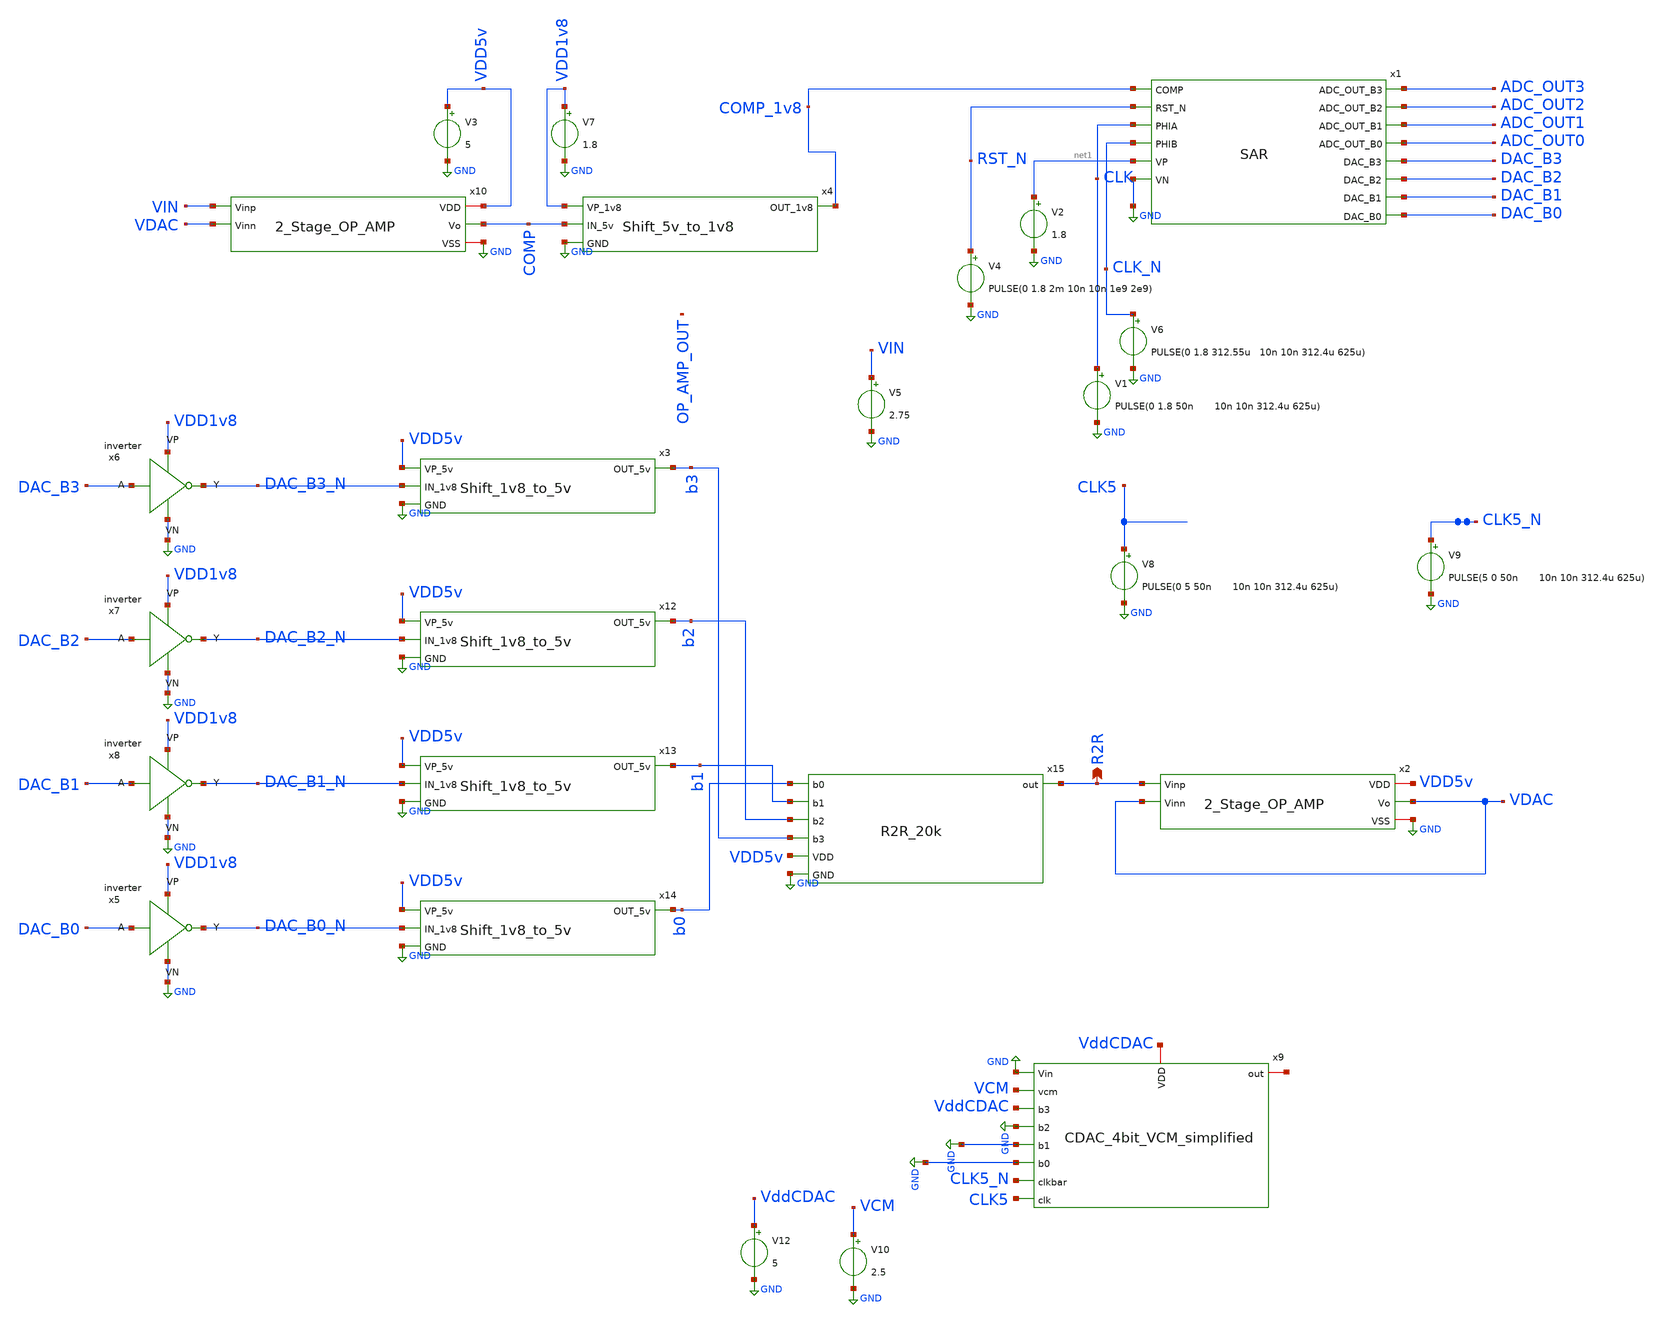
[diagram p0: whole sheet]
** sch_path: ADC/16bit_C2C/MagicAndSpice/EE431_FinalProj/SAR_tb_CY2.sch
**.subckt SAR_tb_CY2 R2R
*.opin R2R
V1 CLK GND PULSE(0 1.8 50n 10n 10n 312.4u 625u)
V2 net1 GND 1.8
V4 RST_N GND PULSE(0 1.8 2m 10n 10n 1e9 2e9)
V5 VIN GND 2.75
V6 CLK_N GND PULSE(0 1.8 312.55u 10n 10n 312.4u 625u)
V3 VDD5v GND 5
V7 VDD1v8 GND 1.8
x10 VDD5v VIN VDAC COMP GND 2_Stage_OP_AMP
x2 VDD5v R2R VDAC VDAC GND 2_Stage_OP_AMP
x4 VDD1v8 COMP_1v8 COMP GND Shift_5v_to_1v8
x3 VDD5v b3 DAC_B3_N GND Shift_1v8_to_5v
x12 VDD5v b2 DAC_B2_N GND Shift_1v8_to_5v
x13 VDD5v b1 DAC_B1_N GND Shift_1v8_to_5v
x14 VDD5v b0 DAC_B0_N GND Shift_1v8_to_5v
x15 R2R b1 b2 b3 b0 VDD5v GND R2R_20k
x5 DAC_B0 DAC_B0_N VDD1v8 GND inverter
x8 DAC_B1 DAC_B1_N VDD1v8 GND inverter
x7 DAC_B2 DAC_B2_N VDD1v8 GND inverter
x6 DAC_B3 DAC_B3_N VDD1v8 GND inverter
x1 COMP_1v8 RST_N CLK CLK_N ADC_OUT3 ADC_OUT2 ADC_OUT1 ADC_OUT0 DAC_B3 DAC_B2 DAC_B1 DAC_B0 net1 GND
+ SAR
x9 CLK5_N CLK5 GND VddCDAC GND GND GND VCM net2 VddCDAC CDAC_4bit_VCM_simplified
V8 CLK5 GND PULSE(0 5 50n 10n 10n 312.4u 625u)
V10 VCM GND 2.5
V12 VddCDAC GND 5
V9 CLK5_N GND PULSE(5 0 50n 10n 10n 312.4u 625u)
**** begin user architecture code
 .lib $::SKYWATER_MODELS/sky130.lib.spice tt


.tran 10000n 10m
.options method=gear reltol=1e-3 cshunt=1f rshunt=1G
.control
run
.endc

**** end user architecture code
**.ends
.GLOBAL GND
.end
